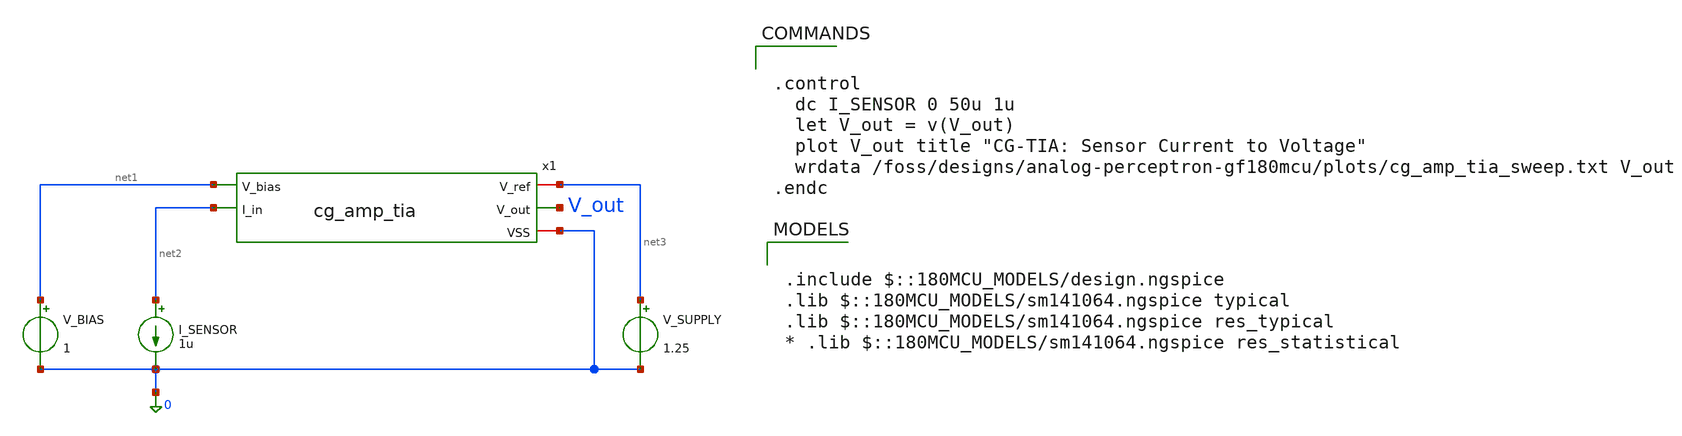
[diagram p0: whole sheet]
** sch_path: schematics/tb_cg_amp_tia.sch
**.subckt tb_cg_amp_tia
x1 net3 V_out net1 net2 0 cg_amp_tia
V_SUPPLY net3 0 1.25
V_BIAS net1 0 1
I_SENSOR net2 0 1u
**** begin user architecture code

.include $::180MCU_MODELS/design.ngspice
.lib $::180MCU_MODELS/sm141064.ngspice typical
.lib $::180MCU_MODELS/sm141064.ngspice res_typical
* .lib $::180MCU_MODELS/sm141064.ngspice res_statistical



.control
  dc I_SENSOR 0 50u 1u
  let V_out = v(V_out)
  plot V_out title "CG-TIA: Sensor Current to Voltage"
  wrdata /foss/designs/analog-perceptron-gf180mcu/plots/cg_amp_tia_sweep.txt V_out
.endc


**** end user architecture code
**.ends

* expanding   symbol:  analog-perceptron-gf180mcu/schematics/cg_amp_tia.sym # of pins=5
** sym_path: schematics/cg_amp_tia.sym
** sch_path: schematics/cg_amp_tia.sch
.subckt cg_amp_tia V_ref V_out V_bias I_in VSS
*.iopin V_ref
*.iopin VSS
*.ipin I_in
*.ipin V_bias
*.opin V_out
XM1 V_out V_bias I_in VSS nfet_03v3 L=0.5u W=5u nf=1 ad='int((nf+1)/2) * W/nf * 0.18u' as='int((nf+2)/2) * W/nf * 0.18u'
+ pd='2*int((nf+1)/2) * (W/nf + 0.18u)' ps='2*int((nf+2)/2) * (W/nf + 0.18u)' nrd='0.18u / W' nrs='0.18u / W'
+ sa=0 sb=0 sd=0 m=1
XR1 V_out V_ref VSS ppolyf_u_1k r_width=3e-6 r_length=8.1e-6 m=1
.ends

.end
